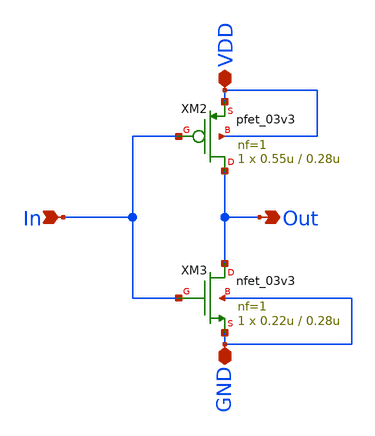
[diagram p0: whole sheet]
** sch_path: xschem/inv.sch
**.subckt inv VDD GND In Out
*.iopin VDD
*.iopin GND
*.ipin In
*.opin Out
XM3 Out In GND GND nfet_03v3 L=0.28u W=0.22u nf=1 ad='int((nf+1)/2) * W/nf * 0.18u' as='int((nf+2)/2) * W/nf * 0.18u'
+ pd='2*int((nf+1)/2) * (W/nf + 0.18u)' ps='2*int((nf+2)/2) * (W/nf + 0.18u)' nrd='0.18u / W' nrs='0.18u / W'
+ sa=0 sb=0 sd=0 m=1
XM2 Out In VDD VDD pfet_03v3 L=0.28u W=0.55u nf=1 ad='int((nf+1)/2) * W/nf * 0.18u' as='int((nf+2)/2) * W/nf * 0.18u'
+ pd='2*int((nf+1)/2) * (W/nf + 0.18u)' ps='2*int((nf+2)/2) * (W/nf + 0.18u)' nrd='0.18u / W' nrs='0.18u / W'
+ sa=0 sb=0 sd=0 m=1
**.ends
.end
